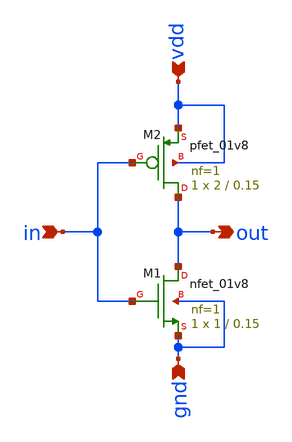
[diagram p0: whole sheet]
** sch_path: Projects/Design_and_Analysis_of_CMOS_Inverter:_Schematic_Design_Layout_Design_and_LVS_Validation_using_SKY130_PDK/assets/files/schematic_design/inverter.sch
**.subckt inverter in vdd gnd out
*.ipin in
*.ipin vdd
*.ipin gnd
*.opin out
XM1 out in gnd gnd sky130_fd_pr__nfet_01v8 L=0.15 W=1 nf=1 ad='int((nf+1)/2) * W/nf * 0.29' as='int((nf+2)/2) * W/nf * 0.29'
+ pd='2*int((nf+1)/2) * (W/nf + 0.29)' ps='2*int((nf+2)/2) * (W/nf + 0.29)' nrd='0.29 / W' nrs='0.29 / W'
+ sa=0 sb=0 sd=0 mult=1 m=1
XM2 out in vdd vdd sky130_fd_pr__pfet_01v8 L=0.15 W=2 nf=1 ad='int((nf+1)/2) * W/nf * 0.29' as='int((nf+2)/2) * W/nf * 0.29'
+ pd='2*int((nf+1)/2) * (W/nf + 0.29)' ps='2*int((nf+2)/2) * (W/nf + 0.29)' nrd='0.29 / W' nrs='0.29 / W'
+ sa=0 sb=0 sd=0 mult=1 m=1
**.ends
.end
